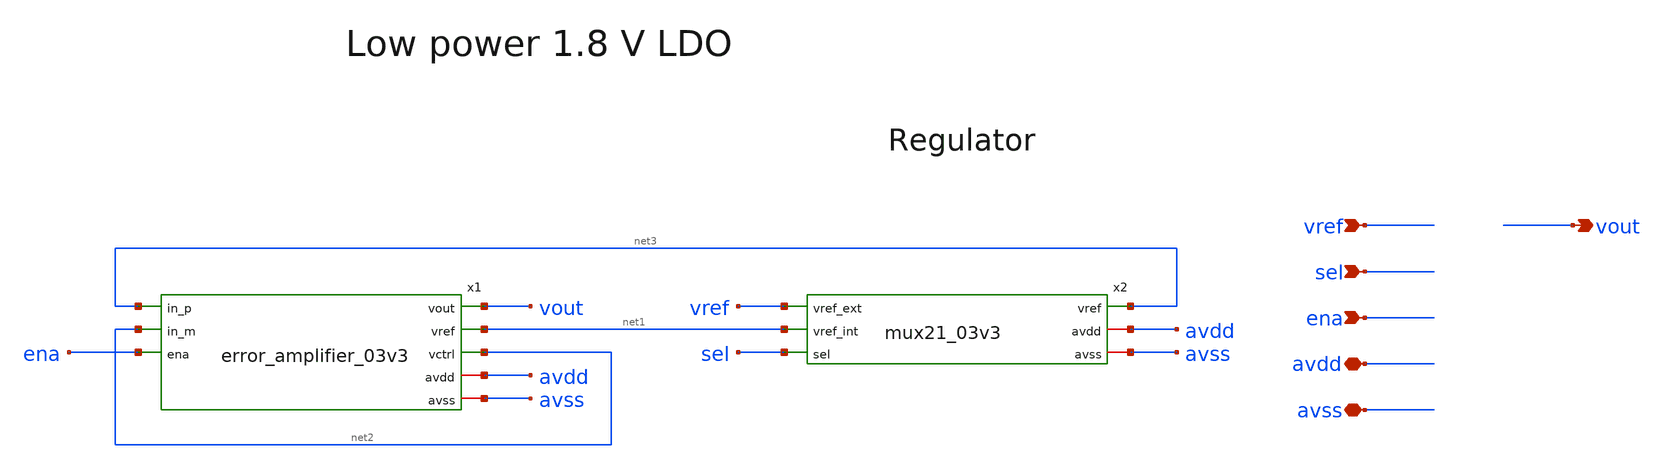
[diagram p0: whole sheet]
** sch_path: xschem/sky130_am_ip__ldo_01v8.sch
**.subckt sky130_am_ip__ldo_01v8 vout ena avdd avss vref sel
*.opin vout
*.ipin ena
*.iopin avdd
*.iopin avss
*.ipin vref
*.ipin sel
x1 net3 vout net1 net2 net2 ena avdd avss error_amplifier_03v3
x2 net3 vref net1 sel avdd avss mux21_03v3
**.ends
.end
